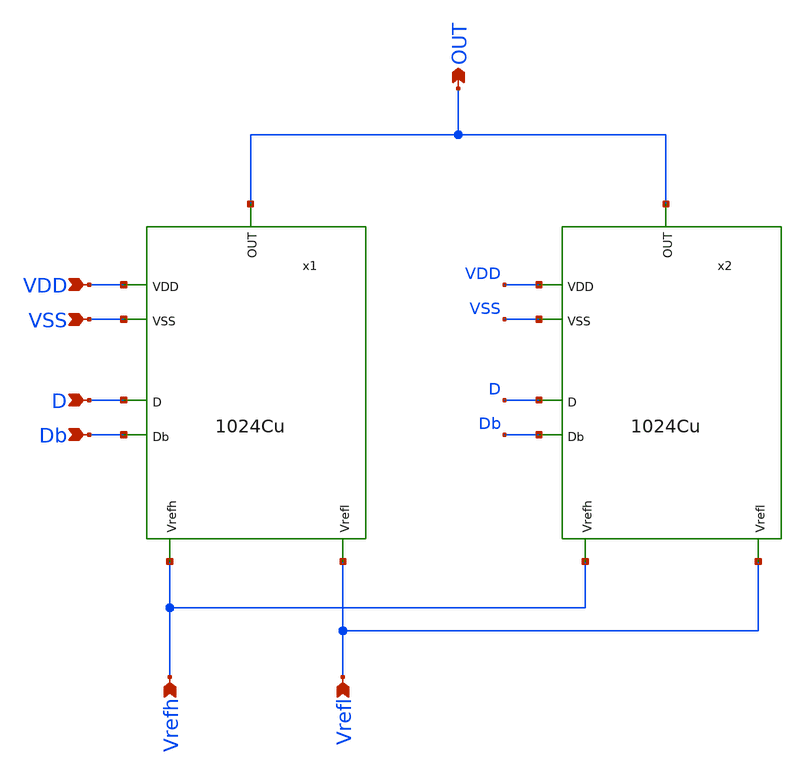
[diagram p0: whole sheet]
** sch_path: 2048Cu.sch
**.subckt 2048Cu OUT VDD D VSS Vrefh Vrefl Db
*.opin OUT
*.ipin VDD
*.ipin D
*.ipin VSS
*.ipin Vrefh
*.ipin Vrefl
*.ipin Db
x1 OUT VSS VDD Db D Vrefl Vrefh 1024Cu
x2 OUT VSS VDD Db D Vrefl Vrefh 1024Cu
**.ends
.end
